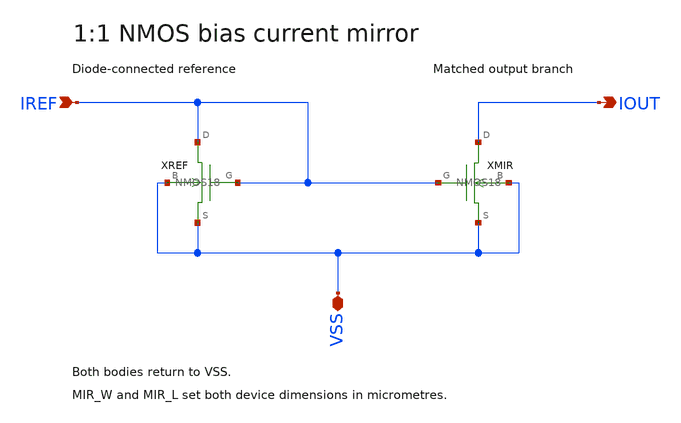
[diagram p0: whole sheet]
** sch_path: examples/sky130-current-mirror/BIAS_MIRROR.sch
**.subckt BIAS_MIRROR IREF IOUT VSS
*.ipin IREF
*.opin IOUT
*.iopin VSS
XREF IREF IREF VSS VSS sky130_fd_pr__nfet_01v8 w='MIR_W' l='MIR_L' nf=1 ad='MIR_W*0.30' as='MIR_W*0.30'
+ pd='2*(MIR_W+0.30)' ps='2*(MIR_W+0.30)'
XMIR IOUT IREF VSS VSS sky130_fd_pr__nfet_01v8 w='MIR_W' l='MIR_L' nf=1 ad='MIR_W*0.30' as='MIR_W*0.30'
+ pd='2*(MIR_W+0.30)' ps='2*(MIR_W+0.30)'
**.ends
.end
